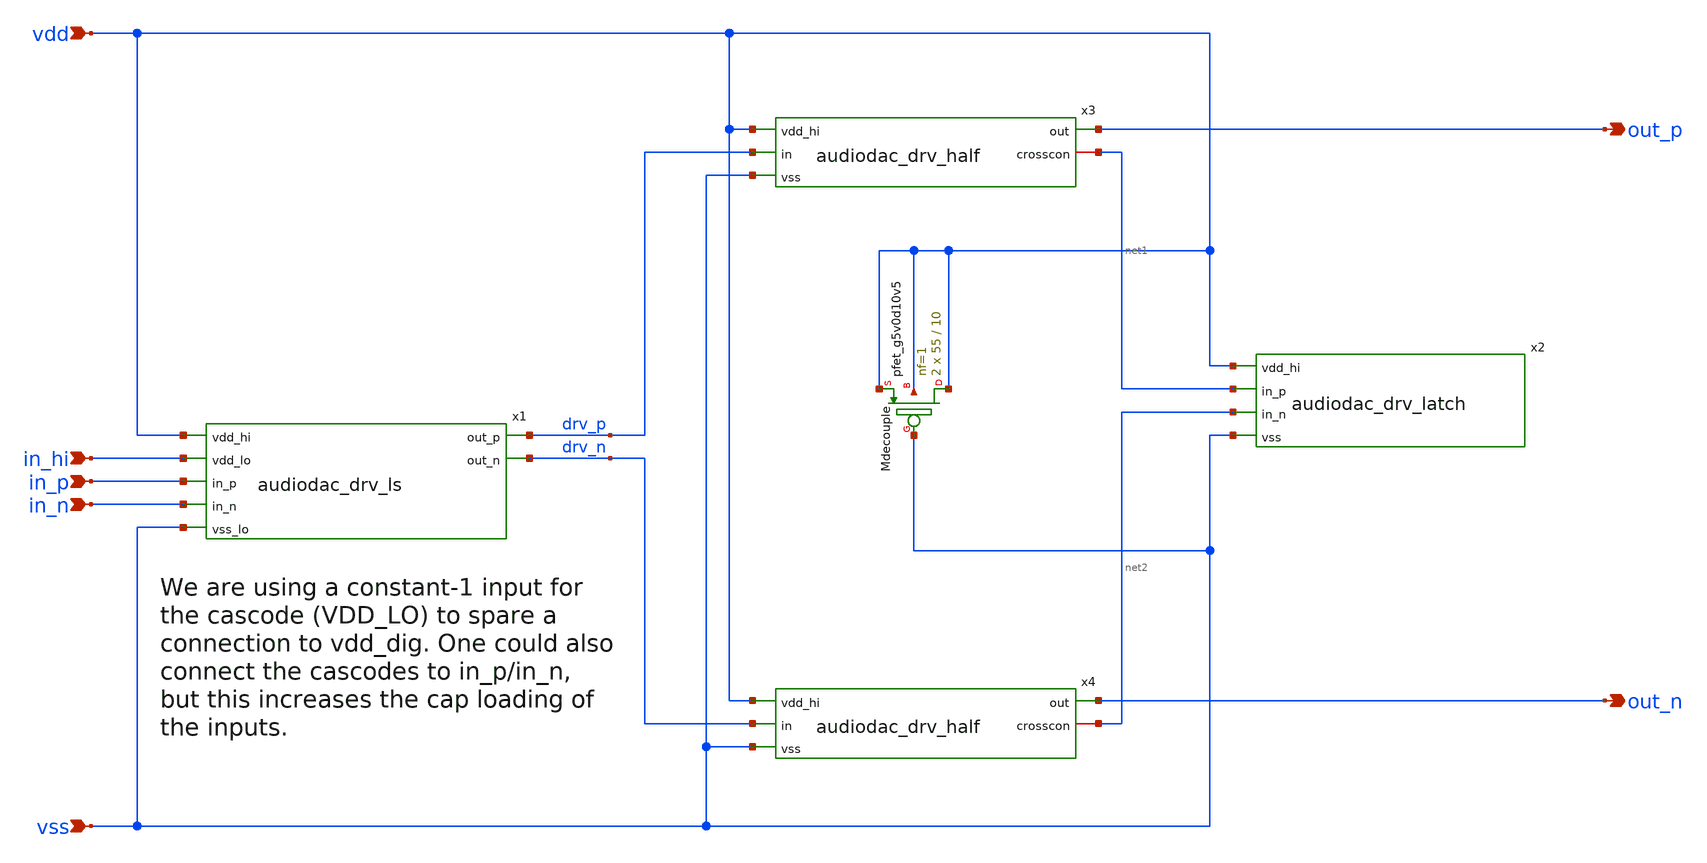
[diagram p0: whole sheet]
** sch_path: xschem/audiodac_drv.sch
* (c) 2022 Harald Pretl, IIC, Johannes Kepler University
**.subckt audiodac_drv in_p in_n out_p out_n vdd in_hi vss
*.ipin in_p
*.ipin in_n
*.opin out_p
*.opin out_n
*.ipin vdd
*.ipin in_hi
*.ipin vss
x1 vdd drv_p drv_n in_hi in_p in_n vss audiodac_drv_ls
x2 vdd net1 net2 vss audiodac_drv_latch
x3 vdd drv_p out_p vss net1 audiodac_drv_half
x4 vdd drv_n out_n vss net2 audiodac_drv_half
XMdecouple vdd vss vdd vdd sky130_fd_pr__pfet_g5v0d10v5 L=10 W=55 nf=1 ad='int((1 + 1)/2) * 55 / 1 * 0.29'
+ as='int((1 + 2)/2) * 55 / 1 * 0.29' pd='2*int((1 + 1)/2) * (55 / 1 + 0.29)' ps='2*int((1 + 2)/2) * (55 / 1 + 0.29)'
+ nrd='0.29 / 55 ' nrs='0.29 / 55 ' sa=0 sb=0 sd=0 mult=2 m=2
**.ends

* expanding   symbol:  audiodac_drv_ls.sym # of pins=7
** sym_path: xschem/audiodac_drv_ls.sym
** sch_path: xschem/audiodac_drv_ls.sch
.subckt audiodac_drv_ls vdd_hi out_p out_n vdd_lo in_p in_n vss_lo
*.ipin in_p
*.ipin in_n
*.opin out_p
*.opin out_n
*.ipin vdd_hi
*.ipin vss_lo
*.ipin vdd_lo
XM6 out_p out_n vdd_hi vdd_hi sky130_fd_pr__pfet_g5v0d10v5 L=0.5 W=10 nf=1 ad='int((1 + 1)/2) * 10 / 1 * 0.29'
+ as='int((1 + 2)/2) * 10 / 1 * 0.29' pd='2*int((1 + 1)/2) * (10 / 1 + 0.29)' ps='2*int((1 + 2)/2) * (10 / 1 + 0.29)'
+ nrd='0.29 / 10 ' nrs='0.29 / 10 ' sa=0 sb=0 sd=0 mult=1 m=1
XM5 out_n out_p vdd_hi vdd_hi sky130_fd_pr__pfet_g5v0d10v5 L=0.5 W=10 nf=1 ad='int((1 + 1)/2) * 10 / 1 * 0.29'
+ as='int((1 + 2)/2) * 10 / 1 * 0.29' pd='2*int((1 + 1)/2) * (10 / 1 + 0.29)' ps='2*int((1 + 2)/2) * (10 / 1 + 0.29)'
+ nrd='0.29 / 10 ' nrs='0.29 / 10 ' sa=0 sb=0 sd=0 mult=1 m=1
XM1 casc1 in_p vss_lo vss_lo sky130_fd_pr__nfet_01v8 L=0.15 W=20 nf=10 ad='int((10 + 1)/2) * 20 / 10 * 0.29'
+ as='int((10 + 2)/2) * 20 / 10 * 0.29' pd='2*int((10 + 1)/2) * (20 / 10 + 0.29)' ps='2*int((10 + 2)/2) * (20 / 10 + 0.29)'
+ nrd='0.29 / 20 ' nrs='0.29 / 20 ' sa=0 sb=0 sd=0 mult=1 m=1
XM2 casc2 in_n vss_lo vss_lo sky130_fd_pr__nfet_01v8 L=0.15 W=20 nf=10 ad='int((10 + 1)/2) * 20 / 10 * 0.29'
+ as='int((10 + 2)/2) * 20 / 10 * 0.29' pd='2*int((10 + 1)/2) * (20 / 10 + 0.29)' ps='2*int((10 + 2)/2) * (20 / 10 + 0.29)'
+ nrd='0.29 / 20 ' nrs='0.29 / 20 ' sa=0 sb=0 sd=0 mult=1 m=1
XM3 out_n vdd_lo casc1 vss_lo sky130_fd_pr__nfet_05v0_nvt L=0.9 W=50 nf=5 ad='int((5 + 1)/2) * 50 / 5 * 0.29'
+ as='int((5 + 2)/2) * 50 / 5 * 0.29' pd='2*int((5 + 1)/2) * (50 / 5 + 0.29)' ps='2*int((5 + 2)/2) * (50 / 5 + 0.29)'
+ nrd='0.29 / 50 ' nrs='0.29 / 50 ' sa=0 sb=0 sd=0 mult=1 m=1
XM4 out_p vdd_lo casc2 vss_lo sky130_fd_pr__nfet_05v0_nvt L=0.9 W=50 nf=5 ad='int((5 + 1)/2) * 50 / 5 * 0.29'
+ as='int((5 + 2)/2) * 50 / 5 * 0.29' pd='2*int((5 + 1)/2) * (50 / 5 + 0.29)' ps='2*int((5 + 2)/2) * (50 / 5 + 0.29)'
+ nrd='0.29 / 50 ' nrs='0.29 / 50 ' sa=0 sb=0 sd=0 mult=1 m=1
.ends


* expanding   symbol:  audiodac_drv_latch.sym # of pins=4
** sym_path: xschem/audiodac_drv_latch.sym
** sch_path: xschem/audiodac_drv_latch.sch
.subckt audiodac_drv_latch vdd_hi in_p in_n vss
*.ipin in_p
*.ipin in_n
*.ipin vdd_hi
*.ipin vss
XM19 in_n in_p vdd_hi vdd_hi sky130_fd_pr__pfet_g5v0d10v5 L=0.5 W=20 nf=2 ad='int((2 + 1)/2) * 20 / 2 * 0.29'
+ as='int((2 + 2)/2) * 20 / 2 * 0.29' pd='2*int((2 + 1)/2) * (20 / 2 + 0.29)' ps='2*int((2 + 2)/2) * (20 / 2 + 0.29)'
+ nrd='0.29 / 20 ' nrs='0.29 / 20 ' sa=0 sb=0 sd=0 mult=1 m=1
XM18 in_n in_p vss vss sky130_fd_pr__nfet_g5v0d10v5 L=0.5 W=10 nf=2 ad='int((2 + 1)/2) * 10 / 2 * 0.29'
+ as='int((2 + 2)/2) * 10 / 2 * 0.29' pd='2*int((2 + 1)/2) * (10 / 2 + 0.29)' ps='2*int((2 + 2)/2) * (10 / 2 + 0.29)'
+ nrd='0.29 / 10 ' nrs='0.29 / 10 ' sa=0 sb=0 sd=0 mult=1 m=1
XM20 in_p in_n vdd_hi vdd_hi sky130_fd_pr__pfet_g5v0d10v5 L=0.5 W=20 nf=2 ad='int((2 + 1)/2) * 20 / 2 * 0.29'
+ as='int((2 + 2)/2) * 20 / 2 * 0.29' pd='2*int((2 + 1)/2) * (20 / 2 + 0.29)' ps='2*int((2 + 2)/2) * (20 / 2 + 0.29)'
+ nrd='0.29 / 20 ' nrs='0.29 / 20 ' sa=0 sb=0 sd=0 mult=1 m=1
XM17 in_p in_n vss vss sky130_fd_pr__nfet_g5v0d10v5 L=0.5 W=10 nf=2 ad='int((2 + 1)/2) * 10 / 2 * 0.29'
+ as='int((2 + 2)/2) * 10 / 2 * 0.29' pd='2*int((2 + 1)/2) * (10 / 2 + 0.29)' ps='2*int((2 + 2)/2) * (10 / 2 + 0.29)'
+ nrd='0.29 / 10 ' nrs='0.29 / 10 ' sa=0 sb=0 sd=0 mult=1 m=1
.ends


* expanding   symbol:  audiodac_drv_half.sym # of pins=5
** sym_path: xschem/audiodac_drv_half.sym
** sch_path: xschem/audiodac_drv_half.sch
.subckt audiodac_drv_half vdd_hi in out vss crosscon
*.ipin in
*.opin out
*.ipin vdd_hi
*.ipin vss
*.iopin crosscon
XM10 out drv4 vdd_hi vdd_hi sky130_fd_pr__pfet_g5v0d10v5 L=0.5 W=100 nf=10 ad='int((10 + 1)/2) * 100 / 10 * 0.29'
+ as='int((10 + 2)/2) * 100 / 10 * 0.29' pd='2*int((10 + 1)/2) * (100 / 10 + 0.29)' ps='2*int((10 + 2)/2) * (100 / 10 + 0.29)'
+ nrd='0.29 / 100 ' nrs='0.29 / 100 ' sa=0 sb=0 sd=0 mult=20 m=20
XM9 out drv4 vss vss sky130_fd_pr__nfet_g5v0d10v5 L=0.5 W=100 nf=10 ad='int((10 + 1)/2) * 100 / 10 * 0.29'
+ as='int((10 + 2)/2) * 100 / 10 * 0.29' pd='2*int((10 + 1)/2) * (100 / 10 + 0.29)' ps='2*int((10 + 2)/2) * (100 / 10 + 0.29)'
+ nrd='0.29 / 100 ' nrs='0.29 / 100 ' sa=0 sb=0 sd=0 mult=10 m=10
XM8 drv4 crosscon vdd_hi vdd_hi sky130_fd_pr__pfet_g5v0d10v5 L=0.5 W=100 nf=10 ad='int((10 + 1)/2) * 100 / 10 * 0.29'
+ as='int((10 + 2)/2) * 100 / 10 * 0.29' pd='2*int((10 + 1)/2) * (100 / 10 + 0.29)' ps='2*int((10 + 2)/2) * (100 / 10 + 0.29)'
+ nrd='0.29 / 100 ' nrs='0.29 / 100 ' sa=0 sb=0 sd=0 mult=2 m=2
XM7 drv4 crosscon vss vss sky130_fd_pr__nfet_g5v0d10v5 L=0.5 W=100 nf=10 ad='int((10 + 1)/2) * 100 / 10 * 0.29'
+ as='int((10 + 2)/2) * 100 / 10 * 0.29' pd='2*int((10 + 1)/2) * (100 / 10 + 0.29)' ps='2*int((10 + 2)/2) * (100 / 10 + 0.29)'
+ nrd='0.29 / 100 ' nrs='0.29 / 100 ' sa=0 sb=0 sd=0 mult=1 m=1
XM6 crosscon drv2 vdd_hi vdd_hi sky130_fd_pr__pfet_g5v0d10v5 L=0.5 W=40 nf=4 ad='int((4 + 1)/2) * 40 / 4 * 0.29'
+ as='int((4 + 2)/2) * 40 / 4 * 0.29' pd='2*int((4 + 1)/2) * (40 / 4 + 0.29)' ps='2*int((4 + 2)/2) * (40 / 4 + 0.29)'
+ nrd='0.29 / 40 ' nrs='0.29 / 40 ' sa=0 sb=0 sd=0 mult=1 m=1
XM5 crosscon drv2 vss vss sky130_fd_pr__nfet_g5v0d10v5 L=0.5 W=20 nf=4 ad='int((4 + 1)/2) * 20 / 4 * 0.29'
+ as='int((4 + 2)/2) * 20 / 4 * 0.29' pd='2*int((4 + 1)/2) * (20 / 4 + 0.29)' ps='2*int((4 + 2)/2) * (20 / 4 + 0.29)'
+ nrd='0.29 / 20 ' nrs='0.29 / 20 ' sa=0 sb=0 sd=0 mult=1 m=1
XM4 drv2 drv1 vdd_hi vdd_hi sky130_fd_pr__pfet_g5v0d10v5 L=0.5 W=8 nf=2 ad='int((2 + 1)/2) * 8 / 2 * 0.29'
+ as='int((2 + 2)/2) * 8 / 2 * 0.29' pd='2*int((2 + 1)/2) * (8 / 2 + 0.29)' ps='2*int((2 + 2)/2) * (8 / 2 + 0.29)'
+ nrd='0.29 / 8 ' nrs='0.29 / 8 ' sa=0 sb=0 sd=0 mult=1 m=1
XM3 drv2 drv1 vss vss sky130_fd_pr__nfet_g5v0d10v5 L=0.5 W=4 nf=1 ad='int((1 + 1)/2) * 4 / 1 * 0.29'
+ as='int((1 + 2)/2) * 4 / 1 * 0.29' pd='2*int((1 + 1)/2) * (4 / 1 + 0.29)' ps='2*int((1 + 2)/2) * (4 / 1 + 0.29)'
+ nrd='0.29 / 4 ' nrs='0.29 / 4 ' sa=0 sb=0 sd=0 mult=1 m=1
XM2 drv1 in vdd_hi vdd_hi sky130_fd_pr__pfet_g5v0d10v5 L=0.5 W=2 nf=2 ad='int((2 + 1)/2) * 2 / 2 * 0.29'
+ as='int((2 + 2)/2) * 2 / 2 * 0.29' pd='2*int((2 + 1)/2) * (2 / 2 + 0.29)' ps='2*int((2 + 2)/2) * (2 / 2 + 0.29)'
+ nrd='0.29 / 2 ' nrs='0.29 / 2 ' sa=0 sb=0 sd=0 mult=1 m=1
XM1 drv1 in vss vss sky130_fd_pr__nfet_g5v0d10v5 L=0.5 W=1 nf=1 ad='int((1 + 1)/2) * 1 / 1 * 0.29' as='int((1 + 2)/2) * 1 / 1 * 0.29'
+ pd='2*int((1 + 1)/2) * (1 / 1 + 0.29)' ps='2*int((1 + 2)/2) * (1 / 1 + 0.29)' nrd='0.29 / 1 ' nrs='0.29 / 1 '
+ sa=0 sb=0 sd=0 mult=1 m=1
.ends

.end
